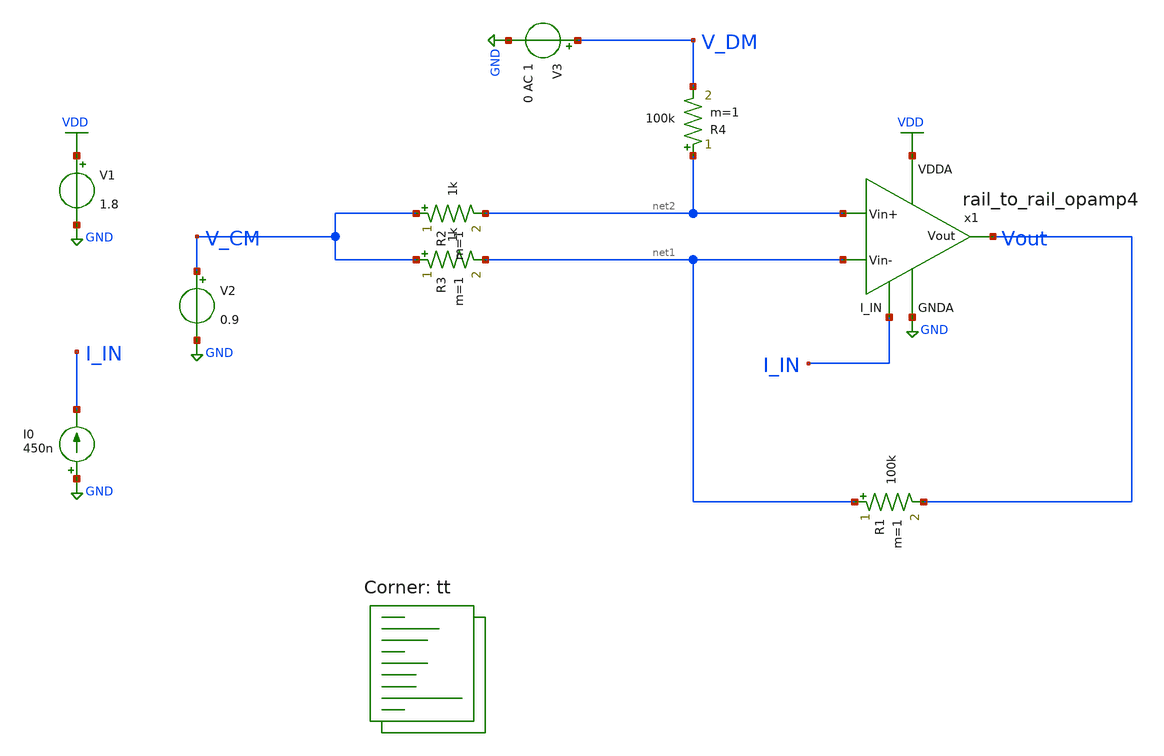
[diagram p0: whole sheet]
** sch_path: projects/pll/charge_pump/xschem_ngspice/tb_rail_to_rail_opamp4.sch
**.subckt tb_rail_to_rail_opamp4
V1 VDD GND 1.8
V3 V_DM GND 0 AC 1
V2 V_CM GND 0.9
R1 net1 Vout 100k m=1
R2 V_CM net2 1k m=1
R3 V_CM net1 1k m=1
R4 net2 V_DM 100k m=1
x1 I_IN VDD net2 net1 Vout GND rail_to_rail_opamp4
I0 GND I_IN 450n
**** begin user architecture code



.option wnflag=1
.option savecurrents

.save @m.x1.xm15.msky130_fd_pr__pfet_01v8[gm] @m.x1.xm14.msky130_fd_pr__pfet_01v8[gm] @m.x1.xm13.msky130_fd_pr__nfet_01v8[gm] @m.x1.xm5.msky130_fd_pr__pfet_01v8[gm] @m.x1.xm4.msky130_fd_pr__pfet_01v8[gm] @m.x1.xm6.msky130_fd_pr__pfet_01v8[gm] @m.x1.xm2.msky130_fd_pr__nfet_01v8[gm] @m.x1.xm3.msky130_fd_pr__nfet_01v8[gm] @m.x1.xm7.msky130_fd_pr__pfet_01v8[gm] @m.x1.xm8.msky130_fd_pr__pfet_01v8[gm] @m.x1.xm1.msky130_fd_pr__nfet_01v8[gm] @m.x1.xm9.msky130_fd_pr__nfet_01v8[gm] @m.x1.xm10.msky130_fd_pr__nfet_01v8[gm] @m.x1.xm11.msky130_fd_pr__pfet_01v8[gm] @m.x1.xm12.msky130_fd_pr__nfet_01v8[gm] @m.x1.xm11.msky130_fd_pr__pfet_01v8[gm] @m.x1.xm17.msky130_fd_pr__nfet_01v8[gm] @m.x1.xm16.msky130_fd_pr__pfet_01v8[gm]

.control
  save all
  * tran 1u 8m
  * ac dec 20 1 1T
  dc V2 0 1.8 0.01
  write tb_rail_to_rail_opamp4_DC.raw
  * write tb_rail_to_rail_opamp4_AC.raw
  * write tb_rail_to_rail_opamp4_tran.raw
  set appendwrite
.endc



.lib $::SKYWATER_MODELS/sky130.lib.spice tt
**** end user architecture code
**.ends

* expanding   symbol:
*+  /foss/designs/my_design/projects/pll/charge_pump/xschem_ngspice/rail_to_rail_opamp4.sym # of pins=6
** sym_path: projects/pll/charge_pump/xschem_ngspice/rail_to_rail_opamp4.sym
** sch_path: projects/pll/charge_pump/xschem_ngspice/rail_to_rail_opamp4.sch
.subckt rail_to_rail_opamp4 I_IN VDDA Vin+ Vin- Vout GNDA
*.opin Vout
*.ipin Vin+
*.ipin Vin-
*.ipin VDDA
*.ipin GNDA
*.ipin I_IN
XM2 n_left Vin+ v_common_n GNDA sky130_fd_pr__nfet_01v8 L=0.15 W=1 nf=2 ad='int((nf+1)/2) * W/nf * 0.29'
+ as='int((nf+2)/2) * W/nf * 0.29' pd='2*int((nf+1)/2) * (W/nf + 0.29)' ps='2*int((nf+2)/2) * (W/nf + 0.29)'
+ nrd='0.29 / W' nrs='0.29 / W' sa=0 sb=0 sd=0 mult=1 m=1
XM3 n_right Vin- v_common_n GNDA sky130_fd_pr__nfet_01v8 L=0.15 W=1 nf=2 ad='int((nf+1)/2) * W/nf * 0.29'
+ as='int((nf+2)/2) * W/nf * 0.29' pd='2*int((nf+1)/2) * (W/nf + 0.29)' ps='2*int((nf+2)/2) * (W/nf + 0.29)'
+ nrd='0.29 / W' nrs='0.29 / W' sa=0 sb=0 sd=0 mult=1 m=1
XM5 n_left n_left VDDA VDDA sky130_fd_pr__pfet_01v8 L=0.15 W=10 nf=20 ad='int((nf+1)/2) * W/nf * 0.29'
+ as='int((nf+2)/2) * W/nf * 0.29' pd='2*int((nf+1)/2) * (W/nf + 0.29)' ps='2*int((nf+2)/2) * (W/nf + 0.29)'
+ nrd='0.29 / W' nrs='0.29 / W' sa=0 sb=0 sd=0 mult=1 m=1
XM4 n_right n_left VDDA VDDA sky130_fd_pr__pfet_01v8 L=0.15 W=10 nf=20 ad='int((nf+1)/2) * W/nf * 0.29'
+ as='int((nf+2)/2) * W/nf * 0.29' pd='2*int((nf+1)/2) * (W/nf + 0.29)' ps='2*int((nf+2)/2) * (W/nf + 0.29)'
+ nrd='0.29 / W' nrs='0.29 / W' sa=0 sb=0 sd=0 mult=1 m=1
XM6 v_common_p p_bias VDDA VDDA sky130_fd_pr__pfet_01v8 L=0.15 W=3 nf=3 ad='int((nf+1)/2) * W/nf * 0.29'
+ as='int((nf+2)/2) * W/nf * 0.29' pd='2*int((nf+1)/2) * (W/nf + 0.29)' ps='2*int((nf+2)/2) * (W/nf + 0.29)'
+ nrd='0.29 / W' nrs='0.29 / W' sa=0 sb=0 sd=0 mult=1 m=1
XM7 p_left Vin+ v_common_p VDDA sky130_fd_pr__pfet_01v8 L=0.15 W=2 nf=2 ad='int((nf+1)/2) * W/nf * 0.29'
+ as='int((nf+2)/2) * W/nf * 0.29' pd='2*int((nf+1)/2) * (W/nf + 0.29)' ps='2*int((nf+2)/2) * (W/nf + 0.29)'
+ nrd='0.29 / W' nrs='0.29 / W' sa=0 sb=0 sd=0 mult=1 m=1
XM8 p_right Vin- v_common_p VDDA sky130_fd_pr__pfet_01v8 L=0.15 W=2 nf=2 ad='int((nf+1)/2) * W/nf * 0.29'
+ as='int((nf+2)/2) * W/nf * 0.29' pd='2*int((nf+1)/2) * (W/nf + 0.29)' ps='2*int((nf+2)/2) * (W/nf + 0.29)'
+ nrd='0.29 / W' nrs='0.29 / W' sa=0 sb=0 sd=0 mult=1 m=1
XM9 p_left p_left GNDA GNDA sky130_fd_pr__nfet_01v8 L=0.15 W=5 nf=10 ad='int((nf+1)/2) * W/nf * 0.29'
+ as='int((nf+2)/2) * W/nf * 0.29' pd='2*int((nf+1)/2) * (W/nf + 0.29)' ps='2*int((nf+2)/2) * (W/nf + 0.29)'
+ nrd='0.29 / W' nrs='0.29 / W' sa=0 sb=0 sd=0 mult=1 m=1
XM10 p_right p_left GNDA GNDA sky130_fd_pr__nfet_01v8 L=0.15 W=5 nf=10 ad='int((nf+1)/2) * W/nf * 0.29'
+ as='int((nf+2)/2) * W/nf * 0.29' pd='2*int((nf+1)/2) * (W/nf + 0.29)' ps='2*int((nf+2)/2) * (W/nf + 0.29)'
+ nrd='0.29 / W' nrs='0.29 / W' sa=0 sb=0 sd=0 mult=1 m=1
XM1 v_common_n I_IN GNDA GNDA sky130_fd_pr__nfet_01v8 L=0.15 W=1 nf=1 ad='int((nf+1)/2) * W/nf * 0.29'
+ as='int((nf+2)/2) * W/nf * 0.29' pd='2*int((nf+1)/2) * (W/nf + 0.29)' ps='2*int((nf+2)/2) * (W/nf + 0.29)'
+ nrd='0.29 / W' nrs='0.29 / W' sa=0 sb=0 sd=0 mult=1 m=1
XM11 Vout n_right VDDA VDDA sky130_fd_pr__pfet_01v8 L=0.15 W=20 nf=40 ad='int((nf+1)/2) * W/nf * 0.29'
+ as='int((nf+2)/2) * W/nf * 0.29' pd='2*int((nf+1)/2) * (W/nf + 0.29)' ps='2*int((nf+2)/2) * (W/nf + 0.29)'
+ nrd='0.29 / W' nrs='0.29 / W' sa=0 sb=0 sd=0 mult=1 m=1
XM12 Vout p_right GNDA GNDA sky130_fd_pr__nfet_01v8 L=0.15 W=10 nf=20 ad='int((nf+1)/2) * W/nf * 0.29'
+ as='int((nf+2)/2) * W/nf * 0.29' pd='2*int((nf+1)/2) * (W/nf + 0.29)' ps='2*int((nf+2)/2) * (W/nf + 0.29)'
+ nrd='0.29 / W' nrs='0.29 / W' sa=0 sb=0 sd=0 mult=1 m=1
XM13 net1 I_IN GNDA GNDA sky130_fd_pr__nfet_01v8 L=0.15 W=1 nf=1 ad='int((nf+1)/2) * W/nf * 0.29' as='int((nf+2)/2) * W/nf * 0.29'
+ pd='2*int((nf+1)/2) * (W/nf + 0.29)' ps='2*int((nf+2)/2) * (W/nf + 0.29)' nrd='0.29 / W' nrs='0.29 / W'
+ sa=0 sb=0 sd=0 mult=1 m=1
XM15 p_bias p_bias VDDA VDDA sky130_fd_pr__pfet_01v8 L=0.15 W=2 nf=2 ad='int((nf+1)/2) * W/nf * 0.29'
+ as='int((nf+2)/2) * W/nf * 0.29' pd='2*int((nf+1)/2) * (W/nf + 0.29)' ps='2*int((nf+2)/2) * (W/nf + 0.29)'
+ nrd='0.29 / W' nrs='0.29 / W' sa=0 sb=0 sd=0 mult=1 m=1
Vmeas p_bias net1 0
.save i(vmeas)
XM14 I_IN I_IN GNDA GNDA sky130_fd_pr__nfet_01v8 L=0.15 W=1 nf=1 ad='int((nf+1)/2) * W/nf * 0.29' as='int((nf+2)/2) * W/nf * 0.29'
+ pd='2*int((nf+1)/2) * (W/nf + 0.29)' ps='2*int((nf+2)/2) * (W/nf + 0.29)' nrd='0.29 / W' nrs='0.29 / W'
+ sa=0 sb=0 sd=0 mult=1 m=1
.ends

.GLOBAL GND
.GLOBAL VDD
.end
